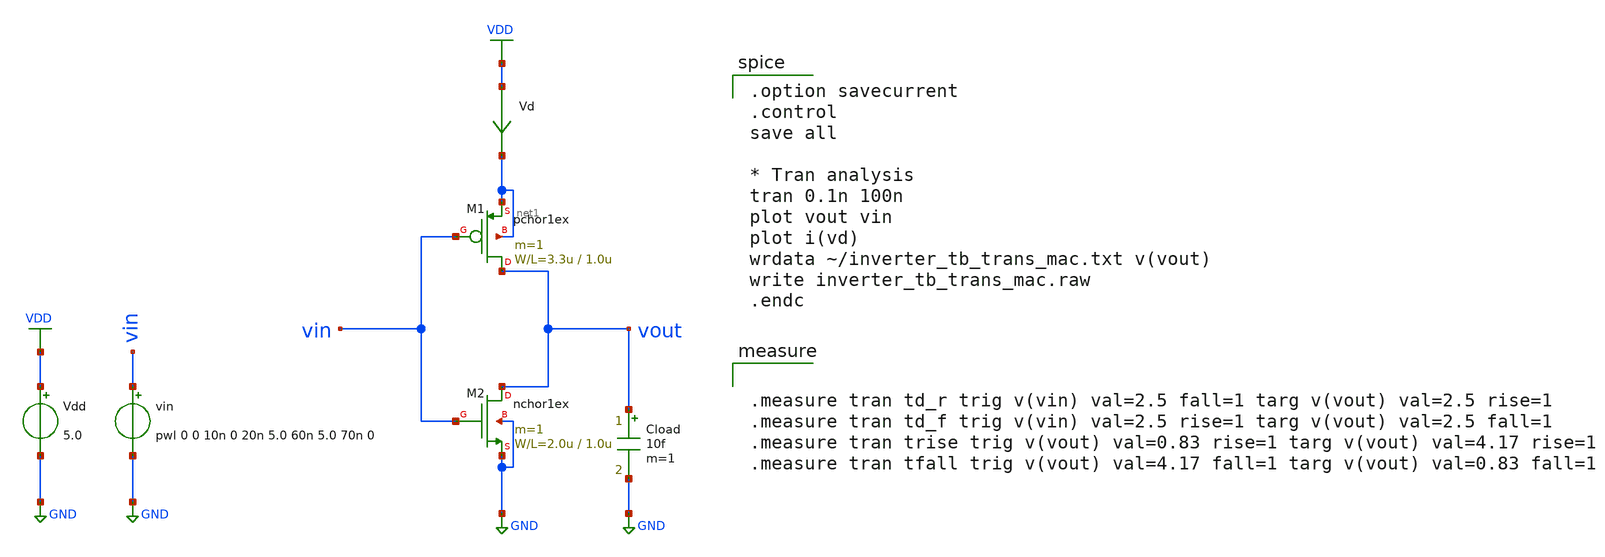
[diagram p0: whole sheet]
** sch_path: samples/inverter/PTS06/inverter_tb_trans_mac.sch
**.subckt inverter_tb_trans_mac
Vdd VDD GND 5.0
vin vin GND pwl 0 0 10n 0 20n 5.0 60n 5.0 70n 0
Vd VDD net1 0
.save i(vd)
Cload vout GND 10f m=1
M1 vout vin net1 net1 pchor1ex L=1.0u W=3.3u m=1
M2 vout vin GND GND nchor1ex L=1.0u W=2.0u m=1
**** begin user architecture code
 .include /Users/noritsuna/.xschem/lib/PTS06/mos.lib
.include /Users/noritsuna/.xschem/lib/PTS06/stdcells.lib

.option savecurrent
.control
save all

* Tran analysis
tran 0.1n 100n
plot vout vin
plot i(vd)
wrdata ~/inverter_tb_trans_mac.txt v(vout)
write inverter_tb_trans_mac.raw
.endc



.measure tran td_r trig v(vin) val=2.5 fall=1 targ v(vout) val=2.5 rise=1
.measure tran td_f trig v(vin) val=2.5 rise=1 targ v(vout) val=2.5 fall=1
.measure tran trise trig v(vout) val=0.83 rise=1 targ v(vout) val=4.17 rise=1
.measure tran tfall trig v(vout) val=4.17 fall=1 targ v(vout) val=0.83 fall=1


**** end user architecture code
**.ends
.GLOBAL VDD
.GLOBAL GND
.end
